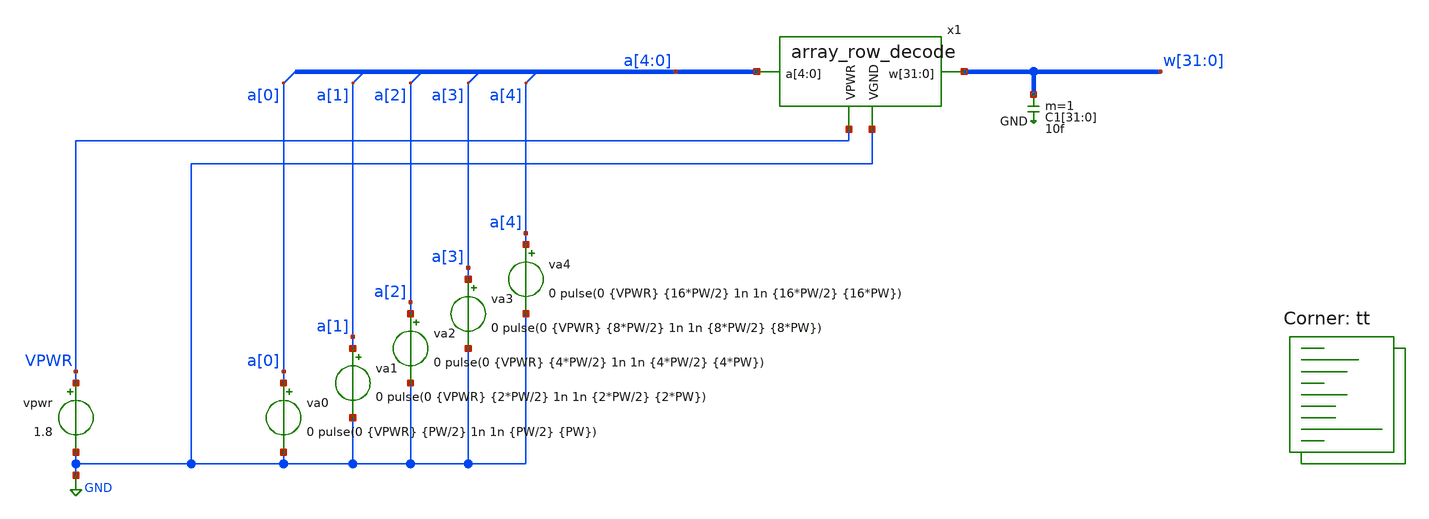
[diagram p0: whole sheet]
** sch_path: xschem/test_array_row_decode.sch
**.subckt test_array_row_decode
x1 VPWR GND a[4] a[3] a[2] a[1] a[0] w[31] w[30] w[29] w[28] w[27] w[26] w[25] w[24] w[23] w[22]
+ w[21] w[20] w[19] w[18] w[17] w[16] w[15] w[14] w[13] w[12] w[11] w[10] w[9] w[8] w[7] w[6] w[5] w[4]
+ w[3] w[2] w[1] w[0] array_row_decode
vpwr VPWR GND 1.8
va0 a[0] GND 0 pulse(0 {VPWR} {PW/2} 1n 1n {PW/2} {PW})
va1 a[1] GND 0 pulse(0 {VPWR} {2*PW/2} 1n 1n {2*PW/2} {2*PW})
va2 a[2] GND 0 pulse(0 {VPWR} {4*PW/2} 1n 1n {4*PW/2} {4*PW})
va3 a[3] GND 0 pulse(0 {VPWR} {8*PW/2} 1n 1n {8*PW/2} {8*PW})
va4 a[4] GND 0 pulse(0 {VPWR} {16*PW/2} 1n 1n {16*PW/2} {16*PW})
C1[31] w[31] GND 10f m=1
C1[30] w[30] GND 10f m=1
C1[29] w[29] GND 10f m=1
C1[28] w[28] GND 10f m=1
C1[27] w[27] GND 10f m=1
C1[26] w[26] GND 10f m=1
C1[25] w[25] GND 10f m=1
C1[24] w[24] GND 10f m=1
C1[23] w[23] GND 10f m=1
C1[22] w[22] GND 10f m=1
C1[21] w[21] GND 10f m=1
C1[20] w[20] GND 10f m=1
C1[19] w[19] GND 10f m=1
C1[18] w[18] GND 10f m=1
C1[17] w[17] GND 10f m=1
C1[16] w[16] GND 10f m=1
C1[15] w[15] GND 10f m=1
C1[14] w[14] GND 10f m=1
C1[13] w[13] GND 10f m=1
C1[12] w[12] GND 10f m=1
C1[11] w[11] GND 10f m=1
C1[10] w[10] GND 10f m=1
C1[9] w[9] GND 10f m=1
C1[8] w[8] GND 10f m=1
C1[7] w[7] GND 10f m=1
C1[6] w[6] GND 10f m=1
C1[5] w[5] GND 10f m=1
C1[4] w[4] GND 10f m=1
C1[3] w[3] GND 10f m=1
C1[2] w[2] GND 10f m=1
C1[1] w[1] GND 10f m=1
C1[0] w[0] GND 10f m=1
**** begin user architecture code
.lib $::SKYWATER_MODELS/sky130.lib.spice tt



.include ../../spice/pex/rcx/array_row_decode.spice
.param VPWR=1.8
.param VSS=0
.param PW=1u
.options savecurrents
.control
  save all
  op
  remzerovec
  write test_array_row_decode.raw
  set appendwrite

  * tran
  tran 10n 50u
  remzerovec
  write test_array_row_decode.raw
.endc



**** end user architecture code
**.ends
.GLOBAL GND
.end
